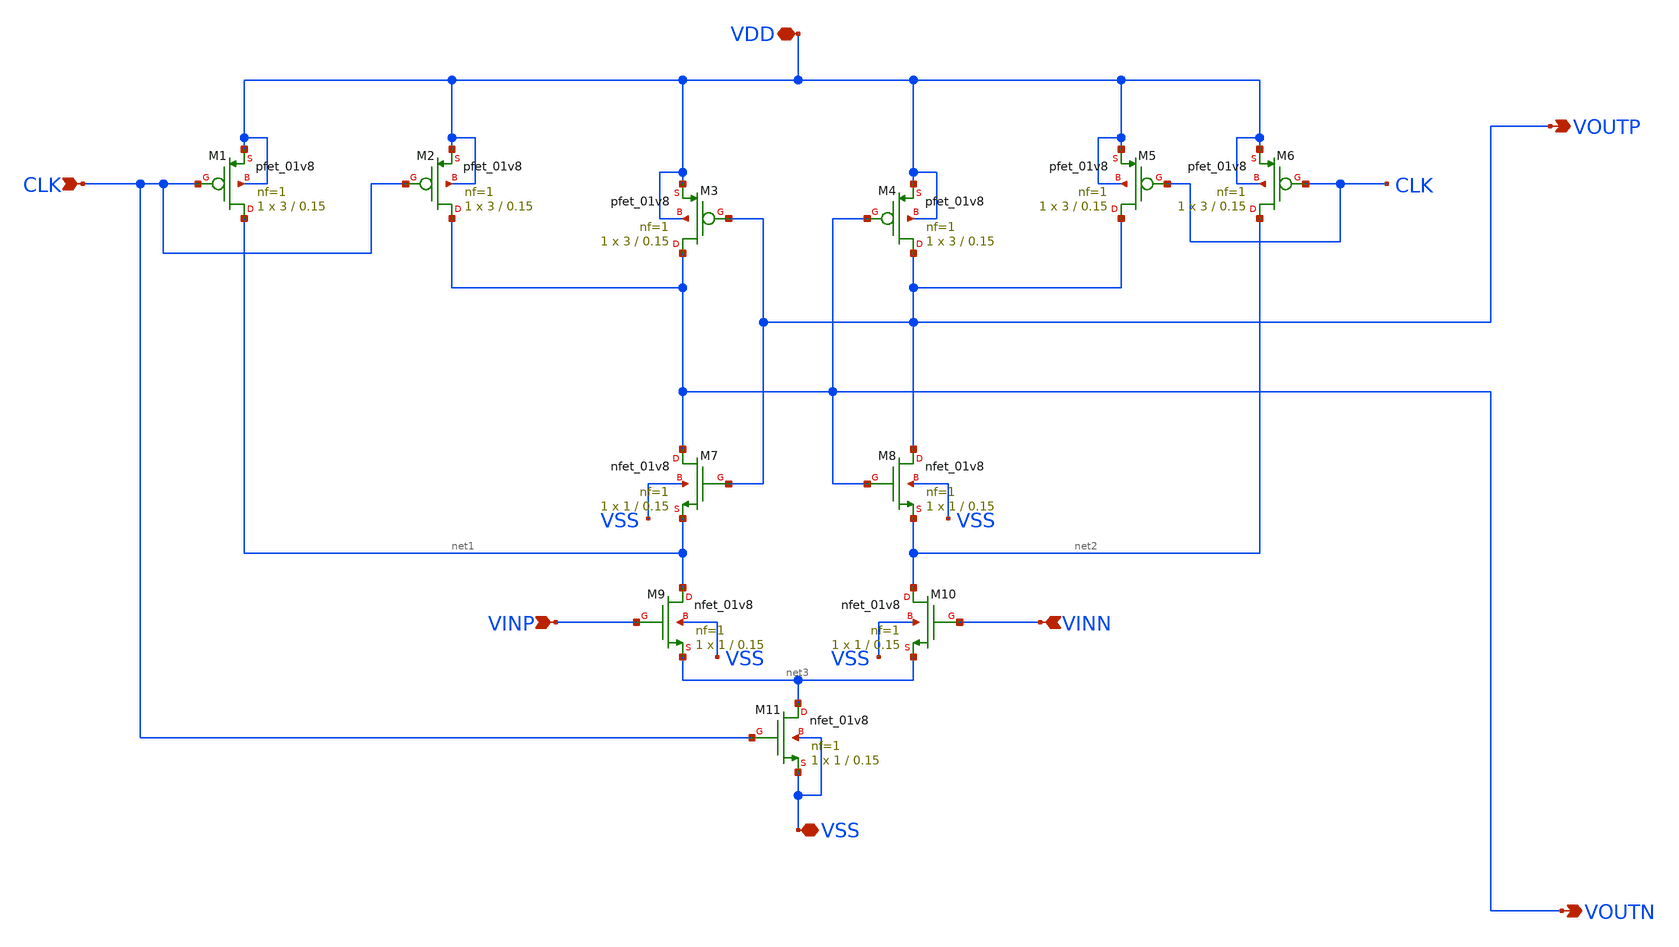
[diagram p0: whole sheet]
** sch_path: SKY130/SAR-ADC/SAR-ADC_1.8V/comp_arm.sch
**.subckt comp_arm VSS VDD CLK VINP VINN VOUTN VOUTP
*.iopin VSS
*.iopin VDD
*.ipin CLK
*.ipin VINP
*.ipin VINN
*.opin VOUTN
*.opin VOUTP
XM1 net1 CLK VDD VDD sky130_fd_pr__pfet_01v8 L=0.15 W=3 nf=1 ad='int((1 + 1)/2) * 3 / 1 * 0.29' as='int((1 + 2)/2) * 3 / 1 * 0.29'
+ pd='2*int((1 + 1)/2) * (3 / 1 + 0.29)' ps='2*int((1 + 2)/2) * (3 / 1 + 0.29)' nrd='0.29 / 3 ' nrs='0.29 / 3 '
+ sa=0 sb=0 sd=0 mult=1 m=1
XM2 VOUTN CLK VDD VDD sky130_fd_pr__pfet_01v8 L=0.15 W=3 nf=1 ad='int((1 + 1)/2) * 3 / 1 * 0.29' as='int((1 + 2)/2) * 3 / 1 * 0.29'
+ pd='2*int((1 + 1)/2) * (3 / 1 + 0.29)' ps='2*int((1 + 2)/2) * (3 / 1 + 0.29)' nrd='0.29 / 3 ' nrs='0.29 / 3 '
+ sa=0 sb=0 sd=0 mult=1 m=1
XM3 VOUTN VOUTP VDD VDD sky130_fd_pr__pfet_01v8 L=0.15 W=3 nf=1 ad='int((1 + 1)/2) * 3 / 1 * 0.29' as='int((1 + 2)/2) * 3 / 1 * 0.29'
+ pd='2*int((1 + 1)/2) * (3 / 1 + 0.29)' ps='2*int((1 + 2)/2) * (3 / 1 + 0.29)' nrd='0.29 / 3 ' nrs='0.29 / 3 '
+ sa=0 sb=0 sd=0 mult=1 m=1
XM4 VOUTP VOUTN VDD VDD sky130_fd_pr__pfet_01v8 L=0.15 W=3 nf=1 ad='int((1 + 1)/2) * 3 / 1 * 0.29' as='int((1 + 2)/2) * 3 / 1 * 0.29'
+ pd='2*int((1 + 1)/2) * (3 / 1 + 0.29)' ps='2*int((1 + 2)/2) * (3 / 1 + 0.29)' nrd='0.29 / 3 ' nrs='0.29 / 3 '
+ sa=0 sb=0 sd=0 mult=1 m=1
XM5 VOUTP CLK VDD VDD sky130_fd_pr__pfet_01v8 L=0.15 W=3 nf=1 ad='int((1 + 1)/2) * 3 / 1 * 0.29' as='int((1 + 2)/2) * 3 / 1 * 0.29'
+ pd='2*int((1 + 1)/2) * (3 / 1 + 0.29)' ps='2*int((1 + 2)/2) * (3 / 1 + 0.29)' nrd='0.29 / 3 ' nrs='0.29 / 3 '
+ sa=0 sb=0 sd=0 mult=1 m=1
XM6 net2 CLK VDD VDD sky130_fd_pr__pfet_01v8 L=0.15 W=3 nf=1 ad='int((1 + 1)/2) * 3 / 1 * 0.29' as='int((1 + 2)/2) * 3 / 1 * 0.29'
+ pd='2*int((1 + 1)/2) * (3 / 1 + 0.29)' ps='2*int((1 + 2)/2) * (3 / 1 + 0.29)' nrd='0.29 / 3 ' nrs='0.29 / 3 '
+ sa=0 sb=0 sd=0 mult=1 m=1
XM7 VOUTN VOUTP net1 VSS sky130_fd_pr__nfet_01v8 L=0.15 W=1 nf=1 ad='int((1 + 1)/2) * 1 / 1 * 0.29' as='int((1 + 2)/2) * 1 / 1 * 0.29'
+ pd='2*int((1 + 1)/2) * (1 / 1 + 0.29)' ps='2*int((1 + 2)/2) * (1 / 1 + 0.29)' nrd='0.29 / 1 ' nrs='0.29 / 1 '
+ sa=0 sb=0 sd=0 mult=1 m=1
XM10 net2 VINN net3 VSS sky130_fd_pr__nfet_01v8 L=0.15 W=1 nf=1 ad='int((1 + 1)/2) * 1 / 1 * 0.29' as='int((1 + 2)/2) * 1 / 1 * 0.29'
+ pd='2*int((1 + 1)/2) * (1 / 1 + 0.29)' ps='2*int((1 + 2)/2) * (1 / 1 + 0.29)' nrd='0.29 / 1 ' nrs='0.29 / 1 '
+ sa=0 sb=0 sd=0 mult=1 m=1
XM8 VOUTP VOUTN net2 VSS sky130_fd_pr__nfet_01v8 L=0.15 W=1 nf=1 ad='int((1 + 1)/2) * 1 / 1 * 0.29' as='int((1 + 2)/2) * 1 / 1 * 0.29'
+ pd='2*int((1 + 1)/2) * (1 / 1 + 0.29)' ps='2*int((1 + 2)/2) * (1 / 1 + 0.29)' nrd='0.29 / 1 ' nrs='0.29 / 1 '
+ sa=0 sb=0 sd=0 mult=1 m=1
XM9 net1 VINP net3 VSS sky130_fd_pr__nfet_01v8 L=0.15 W=1 nf=1 ad='int((1 + 1)/2) * 1 / 1 * 0.29' as='int((1 + 2)/2) * 1 / 1 * 0.29'
+ pd='2*int((1 + 1)/2) * (1 / 1 + 0.29)' ps='2*int((1 + 2)/2) * (1 / 1 + 0.29)' nrd='0.29 / 1 ' nrs='0.29 / 1 '
+ sa=0 sb=0 sd=0 mult=1 m=1
XM11 net3 CLK VSS VSS sky130_fd_pr__nfet_01v8 L=0.15 W=1 nf=1 ad='int((1 + 1)/2) * 1 / 1 * 0.29' as='int((1 + 2)/2) * 1 / 1 * 0.29'
+ pd='2*int((1 + 1)/2) * (1 / 1 + 0.29)' ps='2*int((1 + 2)/2) * (1 / 1 + 0.29)' nrd='0.29 / 1 ' nrs='0.29 / 1 '
+ sa=0 sb=0 sd=0 mult=1 m=1
**.ends
.end
